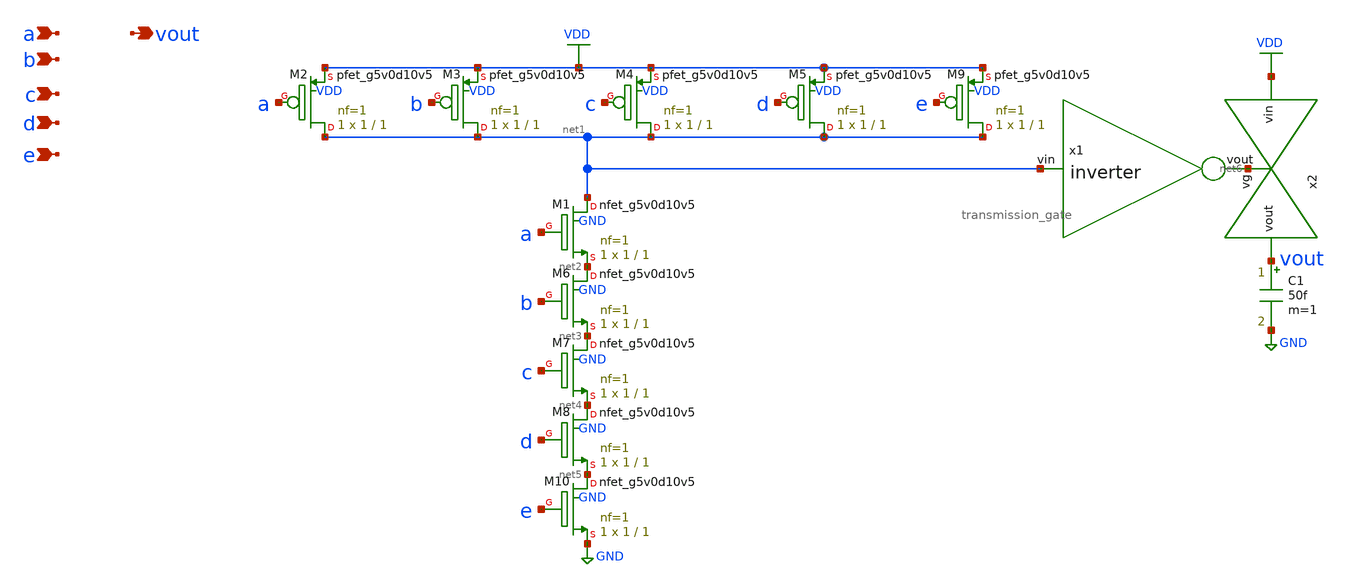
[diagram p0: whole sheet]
** sch_path: schematics/and5.sch
**.subckt and5 a b c d e vout
*.ipin a
*.ipin b
*.ipin c
*.ipin d
*.ipin e
*.opin vout
XM1 net1 a net2 GND sky130_fd_pr__nfet_g5v0d10v5 L=1 W=1 nf=1 ad='int((nf+1)/2) * W/nf * 0.29' as='int((nf+2)/2) * W/nf * 0.29'
+ pd='2*int((nf+1)/2) * (W/nf + 0.29)' ps='2*int((nf+2)/2) * (W/nf + 0.29)' nrd='0.29 / W' nrs='0.29 / W'
+ sa=0 sb=0 sd=0 mult=1 m=1
XM2 net1 a VDD VDD sky130_fd_pr__pfet_g5v0d10v5 L=1 W=1 nf=1 ad='int((nf+1)/2) * W/nf * 0.29' as='int((nf+2)/2) * W/nf * 0.29'
+ pd='2*int((nf+1)/2) * (W/nf + 0.29)' ps='2*int((nf+2)/2) * (W/nf + 0.29)' nrd='0.29 / W' nrs='0.29 / W'
+ sa=0 sb=0 sd=0 mult=1 m=1
XM3 net1 b VDD VDD sky130_fd_pr__pfet_g5v0d10v5 L=1 W=1 nf=1 ad='int((nf+1)/2) * W/nf * 0.29' as='int((nf+2)/2) * W/nf * 0.29'
+ pd='2*int((nf+1)/2) * (W/nf + 0.29)' ps='2*int((nf+2)/2) * (W/nf + 0.29)' nrd='0.29 / W' nrs='0.29 / W'
+ sa=0 sb=0 sd=0 mult=1 m=1
XM4 net1 c VDD VDD sky130_fd_pr__pfet_g5v0d10v5 L=1 W=1 nf=1 ad='int((nf+1)/2) * W/nf * 0.29' as='int((nf+2)/2) * W/nf * 0.29'
+ pd='2*int((nf+1)/2) * (W/nf + 0.29)' ps='2*int((nf+2)/2) * (W/nf + 0.29)' nrd='0.29 / W' nrs='0.29 / W'
+ sa=0 sb=0 sd=0 mult=1 m=1
XM5 net1 d VDD VDD sky130_fd_pr__pfet_g5v0d10v5 L=1 W=1 nf=1 ad='int((nf+1)/2) * W/nf * 0.29' as='int((nf+2)/2) * W/nf * 0.29'
+ pd='2*int((nf+1)/2) * (W/nf + 0.29)' ps='2*int((nf+2)/2) * (W/nf + 0.29)' nrd='0.29 / W' nrs='0.29 / W'
+ sa=0 sb=0 sd=0 mult=1 m=1
XM6 net2 b net3 GND sky130_fd_pr__nfet_g5v0d10v5 L=1 W=1 nf=1 ad='int((nf+1)/2) * W/nf * 0.29' as='int((nf+2)/2) * W/nf * 0.29'
+ pd='2*int((nf+1)/2) * (W/nf + 0.29)' ps='2*int((nf+2)/2) * (W/nf + 0.29)' nrd='0.29 / W' nrs='0.29 / W'
+ sa=0 sb=0 sd=0 mult=1 m=1
XM7 net3 c net4 GND sky130_fd_pr__nfet_g5v0d10v5 L=1 W=1 nf=1 ad='int((nf+1)/2) * W/nf * 0.29' as='int((nf+2)/2) * W/nf * 0.29'
+ pd='2*int((nf+1)/2) * (W/nf + 0.29)' ps='2*int((nf+2)/2) * (W/nf + 0.29)' nrd='0.29 / W' nrs='0.29 / W'
+ sa=0 sb=0 sd=0 mult=1 m=1
XM8 net4 d net5 GND sky130_fd_pr__nfet_g5v0d10v5 L=1 W=1 nf=1 ad='int((nf+1)/2) * W/nf * 0.29' as='int((nf+2)/2) * W/nf * 0.29'
+ pd='2*int((nf+1)/2) * (W/nf + 0.29)' ps='2*int((nf+2)/2) * (W/nf + 0.29)' nrd='0.29 / W' nrs='0.29 / W'
+ sa=0 sb=0 sd=0 mult=1 m=1
x1 net6 net1 inverter
XM9 net1 e VDD VDD sky130_fd_pr__pfet_g5v0d10v5 L=1 W=1 nf=1 ad='int((nf+1)/2) * W/nf * 0.29' as='int((nf+2)/2) * W/nf * 0.29'
+ pd='2*int((nf+1)/2) * (W/nf + 0.29)' ps='2*int((nf+2)/2) * (W/nf + 0.29)' nrd='0.29 / W' nrs='0.29 / W'
+ sa=0 sb=0 sd=0 mult=1 m=1
XM10 net5 e GND GND sky130_fd_pr__nfet_g5v0d10v5 L=1 W=1 nf=1 ad='int((nf+1)/2) * W/nf * 0.29' as='int((nf+2)/2) * W/nf * 0.29'
+ pd='2*int((nf+1)/2) * (W/nf + 0.29)' ps='2*int((nf+2)/2) * (W/nf + 0.29)' nrd='0.29 / W' nrs='0.29 / W'
+ sa=0 sb=0 sd=0 mult=1 m=1
x2 VDD vout net6 transmission_gate
C1 vout GND 50f m=1
**.ends

* expanding   symbol:  /media/sf_share/final_project/inverter.sym # of pins=2
** sym_path: schematics/inverter.sym
** sch_path: schematics/inverter.sch
.subckt inverter vout vin
*.ipin vin
*.opin vout
XM3 vout vin VDD VDD sky130_fd_pr__pfet_g5v0d10v5 L=0.5 W=0.5 nf=1 ad='int((nf+1)/2) * W/nf * 0.29' as='int((nf+2)/2) * W/nf * 0.29'
+ pd='2*int((nf+1)/2) * (W/nf + 0.29)' ps='2*int((nf+2)/2) * (W/nf + 0.29)' nrd='0.29 / W' nrs='0.29 / W'
+ sa=0 sb=0 sd=0 mult=1 m=1
XM5 vout vin GND GND sky130_fd_pr__nfet_g5v0d10v5 L=0.5 W=0.5 nf=1 ad='int((nf+1)/2) * W/nf * 0.29' as='int((nf+2)/2) * W/nf * 0.29'
+ pd='2*int((nf+1)/2) * (W/nf + 0.29)' ps='2*int((nf+2)/2) * (W/nf + 0.29)' nrd='0.29 / W' nrs='0.29 / W'
+ sa=0 sb=0 sd=0 mult=1 m=1
.ends


* expanding   symbol:  /media/sf_share/final_project/transmission_gate.sym # of pins=3
** sym_path: schematics/transmission_gate.sym
** sch_path: schematics/transmission_gate.sch
.subckt transmission_gate vin vout vg
*.ipin vin
*.ipin vg
*.opin vout
x1 vg_bar vg inverter
XM5 vin vg vout GND sky130_fd_pr__nfet_g5v0d10v5 L=0.5 W=0.5 nf=1 ad='int((nf+1)/2) * W/nf * 0.29' as='int((nf+2)/2) * W/nf * 0.29'
+ pd='2*int((nf+1)/2) * (W/nf + 0.29)' ps='2*int((nf+2)/2) * (W/nf + 0.29)' nrd='0.29 / W' nrs='0.29 / W'
+ sa=0 sb=0 sd=0 mult=1 m=1
XM7 vout vg_bar vin VDD sky130_fd_pr__pfet_g5v0d10v5 L=0.5 W=0.5 nf=1 ad='int((nf+1)/2) * W/nf * 0.29'
+ as='int((nf+2)/2) * W/nf * 0.29' pd='2*int((nf+1)/2) * (W/nf + 0.29)' ps='2*int((nf+2)/2) * (W/nf + 0.29)'
+ nrd='0.29 / W' nrs='0.29 / W' sa=0 sb=0 sd=0 mult=1 m=1
XM6 vout vg_bar GND GND sky130_fd_pr__nfet_g5v0d10v5 L=0.5 W=0.5 nf=1 ad='int((nf+1)/2) * W/nf * 0.29'
+ as='int((nf+2)/2) * W/nf * 0.29' pd='2*int((nf+1)/2) * (W/nf + 0.29)' ps='2*int((nf+2)/2) * (W/nf + 0.29)'
+ nrd='0.29 / W' nrs='0.29 / W' sa=0 sb=0 sd=0 mult=1 m=1
.ends

.GLOBAL GND
.GLOBAL VDD
.end
